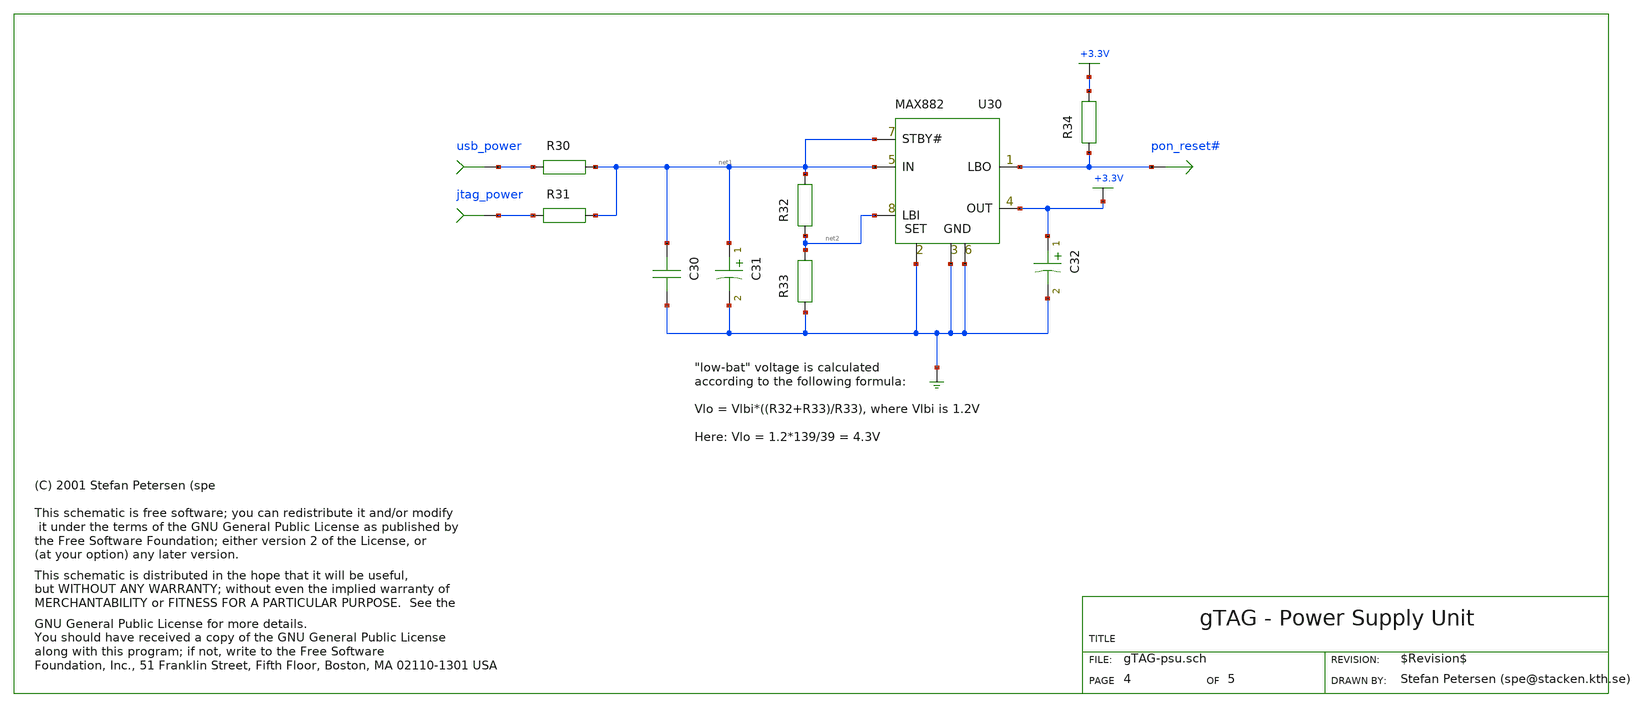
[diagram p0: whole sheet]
** sch_path: xschem-src/xschem_library/gschem_import/gTAG-psu.sch
* Copyright (C) 1998-2026 Stefan Frederik Schippers
* This program is free software; you can redistribute it and/or modify
* it under the terms of the GNU General Public License as published by
* the Free Software Foundation; either version 2 of the License, or
* (at your option) any later version.
* This program is distributed in the hope that it will be useful,
* but WITHOUT ANY WARRANTY; without even the implied warranty of
* MERCHANTABILITY or FITNESS FOR A PARTICULAR PURPOSE.  See the
* GNU General Public License for more details.
* You should have received a copy of the GNU General Public License
* along with this program; if not, write to the Free Software
* copyleft.sym
**.subckt gTAG-psu usb_power jtag_power pon_reset#
U30 net1 net1 net2 GND GND GND +3.3V pon_reset#
C32 +3.3V GND 2.2u
C31 net1 GND 2.2u
R30 usb_power net1 0
R31 jtag_power net1 0
C30 net1 GND 100n
C30
R33 GND net2 39k
R32 net2 net1 100k
R34 pon_reset# +3.3V 10k
**.ends
.end
